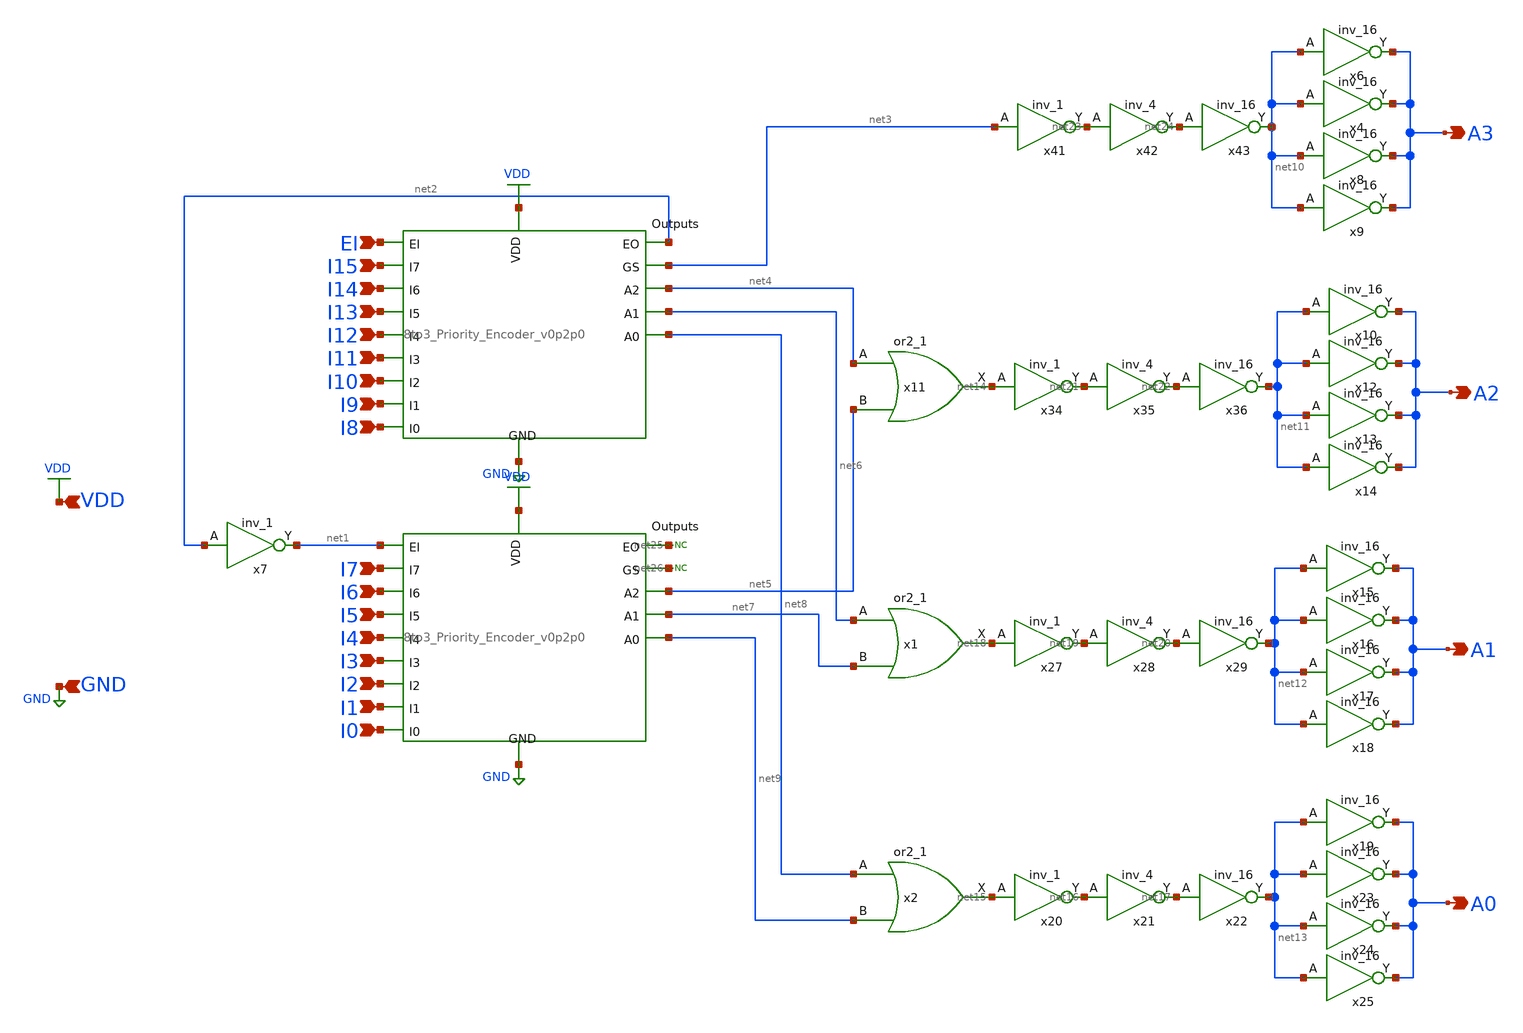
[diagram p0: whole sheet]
** sch_path: PriorityEncoder/xschem/16to4_PriorityEncoder_v0p0p1.sch
.lib $::SKYWATER_MODELS/sky130.lib.spice tt
.include $::SKYWATER_STDCELLS/sky130_fd_sc_hd.spice

**.subckt 16to4_PriorityEncoder_v0p0p1 I14 I13 I12 I11 I10 I9 I8 I7 I6 I5 I4 I3 I2 I1 I0 A3 I15 EI
*+ A2 A1 A0 VDD GND
*.ipin I14
*.ipin I13
*.ipin I12
*.ipin I11
*.ipin I10
*.ipin I9
*.ipin I8
*.ipin I7
*.ipin I6
*.ipin I5
*.ipin I4
*.ipin I3
*.ipin I2
*.ipin I1
*.ipin I0
*.opin A3
*.ipin I15
*.ipin EI
*.opin A2
*.opin A1
*.opin A0
*.ipin VDD
*.ipin GND
x11 net4 net5 GND GND VDD VDD net14 sky130_fd_sc_hd__or2_1
x20 net15 GND GND VDD VDD net16 sky130_fd_sc_hd__inv_1
x21 net16 GND GND VDD VDD net17 sky130_fd_sc_hd__inv_4
x22 net17 GND GND VDD VDD net13 sky130_fd_sc_hd__inv_16
x27 net18 GND GND VDD VDD net19 sky130_fd_sc_hd__inv_1
x28 net19 GND GND VDD VDD net20 sky130_fd_sc_hd__inv_4
x29 net20 GND GND VDD VDD net12 sky130_fd_sc_hd__inv_16
x34 net14 GND GND VDD VDD net21 sky130_fd_sc_hd__inv_1
x35 net21 GND GND VDD VDD net22 sky130_fd_sc_hd__inv_4
x36 net22 GND GND VDD VDD net11 sky130_fd_sc_hd__inv_16
x41 net3 GND GND VDD VDD net23 sky130_fd_sc_hd__inv_1
x42 net23 GND GND VDD VDD net24 sky130_fd_sc_hd__inv_4
x43 net24 GND GND VDD VDD net10 sky130_fd_sc_hd__inv_16
x7 net2 GND GND VDD VDD net1 sky130_fd_sc_hd__inv_1
x1 net6 net7 GND GND VDD VDD net18 sky130_fd_sc_hd__or2_1
x2 net8 net9 GND GND VDD VDD net15 sky130_fd_sc_hd__or2_1
* noconn #net25
* noconn #net26
x5 I9 I13 I11 I8 I10 I14 I15 I12 net2 net3 net4 net6 net8 EI VDD GND 8to3_Priority_Encoder_v0p2p0
x3 I1 I5 I3 I0 I2 I6 I7 I4 net25 net26 net5 net7 net9 net1 VDD GND 8to3_Priority_Encoder_v0p2p0
x6 net10 GND GND VDD VDD A3 sky130_fd_sc_hd__inv_16
x4 net10 GND GND VDD VDD A3 sky130_fd_sc_hd__inv_16
x8 net10 GND GND VDD VDD A3 sky130_fd_sc_hd__inv_16
x9 net10 GND GND VDD VDD A3 sky130_fd_sc_hd__inv_16
x10 net11 GND GND VDD VDD A2 sky130_fd_sc_hd__inv_16
x12 net11 GND GND VDD VDD A2 sky130_fd_sc_hd__inv_16
x13 net11 GND GND VDD VDD A2 sky130_fd_sc_hd__inv_16
x14 net11 GND GND VDD VDD A2 sky130_fd_sc_hd__inv_16
x15 net12 GND GND VDD VDD A1 sky130_fd_sc_hd__inv_16
x16 net12 GND GND VDD VDD A1 sky130_fd_sc_hd__inv_16
x17 net12 GND GND VDD VDD A1 sky130_fd_sc_hd__inv_16
x18 net12 GND GND VDD VDD A1 sky130_fd_sc_hd__inv_16
x19 net13 GND GND VDD VDD A0 sky130_fd_sc_hd__inv_16
x23 net13 GND GND VDD VDD A0 sky130_fd_sc_hd__inv_16
x24 net13 GND GND VDD VDD A0 sky130_fd_sc_hd__inv_16
x25 net13 GND GND VDD VDD A0 sky130_fd_sc_hd__inv_16
**.ends
.GLOBAL VDD
.GLOBAL GND
.end
